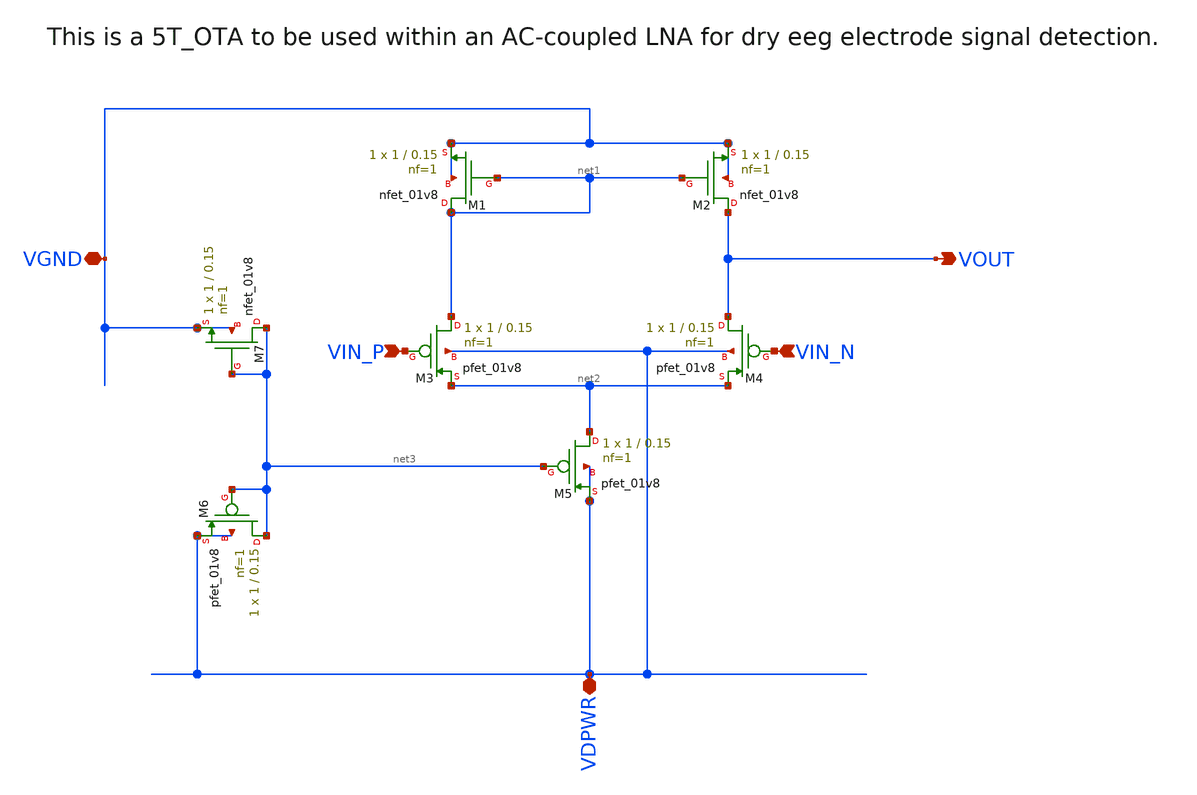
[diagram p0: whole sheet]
** sch_path: xschem/5t_ota.sch
**.subckt 5t_ota VGND VIN_N VIN_P VDPWR VOUT
*.iopin VGND
*.ipin VIN_N
*.ipin VIN_P
*.iopin VDPWR
*.opin VOUT
MM1 net1 net1 VGND VGND sky130_fd_pr__nfet_01v8 L=0.15 W=1 nf=1 ad='int((1 + 1)/2) * 1 / 1 * 0.29' as='int((1 + 2)/2) * 1 / 1 * 0.29'
+ pd='2*int((1 + 1)/2) * (1 / 1 + 0.29)' ps='2*int((1 + 2)/2) * (1 / 1 + 0.29)' nrd='0.29 / 1 ' nrs='0.29 / 1 '
+ sa=0 sb=0 sd=0 mult=1 m=1
MM2 VOUT net1 VGND VGND sky130_fd_pr__nfet_01v8 L=0.15 W=1 nf=1 ad='int((1 + 1)/2) * 1 / 1 * 0.29' as='int((1 + 2)/2) * 1 / 1 * 0.29'
+ pd='2*int((1 + 1)/2) * (1 / 1 + 0.29)' ps='2*int((1 + 2)/2) * (1 / 1 + 0.29)' nrd='0.29 / 1 ' nrs='0.29 / 1 '
+ sa=0 sb=0 sd=0 mult=1 m=1
MM3 net1 VIN_P net2 VDPWR sky130_fd_pr__pfet_01v8 L=0.15 W=1 nf=1 ad='int((1 + 1)/2) * 1 / 1 * 0.29'
+ as='int((1 + 2)/2) * 1 / 1 * 0.29' pd='2*int((1 + 1)/2) * (1 / 1 + 0.29)' ps='2*int((1 + 2)/2) * (1 / 1 + 0.29)'
+ nrd='0.29 / 1 ' nrs='0.29 / 1 ' sa=0 sb=0 sd=0 mult=1 m=1
MM4 VOUT VIN_N net2 VDPWR sky130_fd_pr__pfet_01v8 L=0.15 W=1 nf=1 ad='int((1 + 1)/2) * 1 / 1 * 0.29'
+ as='int((1 + 2)/2) * 1 / 1 * 0.29' pd='2*int((1 + 1)/2) * (1 / 1 + 0.29)' ps='2*int((1 + 2)/2) * (1 / 1 + 0.29)'
+ nrd='0.29 / 1 ' nrs='0.29 / 1 ' sa=0 sb=0 sd=0 mult=1 m=1
MM5 net2 net3 VDPWR VDPWR sky130_fd_pr__pfet_01v8 L=0.15 W=1 nf=1 ad='int((1 + 1)/2) * 1 / 1 * 0.29'
+ as='int((1 + 2)/2) * 1 / 1 * 0.29' pd='2*int((1 + 1)/2) * (1 / 1 + 0.29)' ps='2*int((1 + 2)/2) * (1 / 1 + 0.29)'
+ nrd='0.29 / 1 ' nrs='0.29 / 1 ' sa=0 sb=0 sd=0 mult=1 m=1
MM6 net3 net3 VDPWR VDPWR sky130_fd_pr__pfet_01v8 L=0.15 W=1 nf=1 ad='int((1 + 1)/2) * 1 / 1 * 0.29'
+ as='int((1 + 2)/2) * 1 / 1 * 0.29' pd='2*int((1 + 1)/2) * (1 / 1 + 0.29)' ps='2*int((1 + 2)/2) * (1 / 1 + 0.29)'
+ nrd='0.29 / 1 ' nrs='0.29 / 1 ' sa=0 sb=0 sd=0 mult=1 m=1
MM7 net3 net3 VGND VGND sky130_fd_pr__nfet_01v8 L=0.15 W=1 nf=1 ad='int((1 + 1)/2) * 1 / 1 * 0.29' as='int((1 + 2)/2) * 1 / 1 * 0.29'
+ pd='2*int((1 + 1)/2) * (1 / 1 + 0.29)' ps='2*int((1 + 2)/2) * (1 / 1 + 0.29)' nrd='0.29 / 1 ' nrs='0.29 / 1 '
+ sa=0 sb=0 sd=0 mult=1 m=1
**.ends
.end
